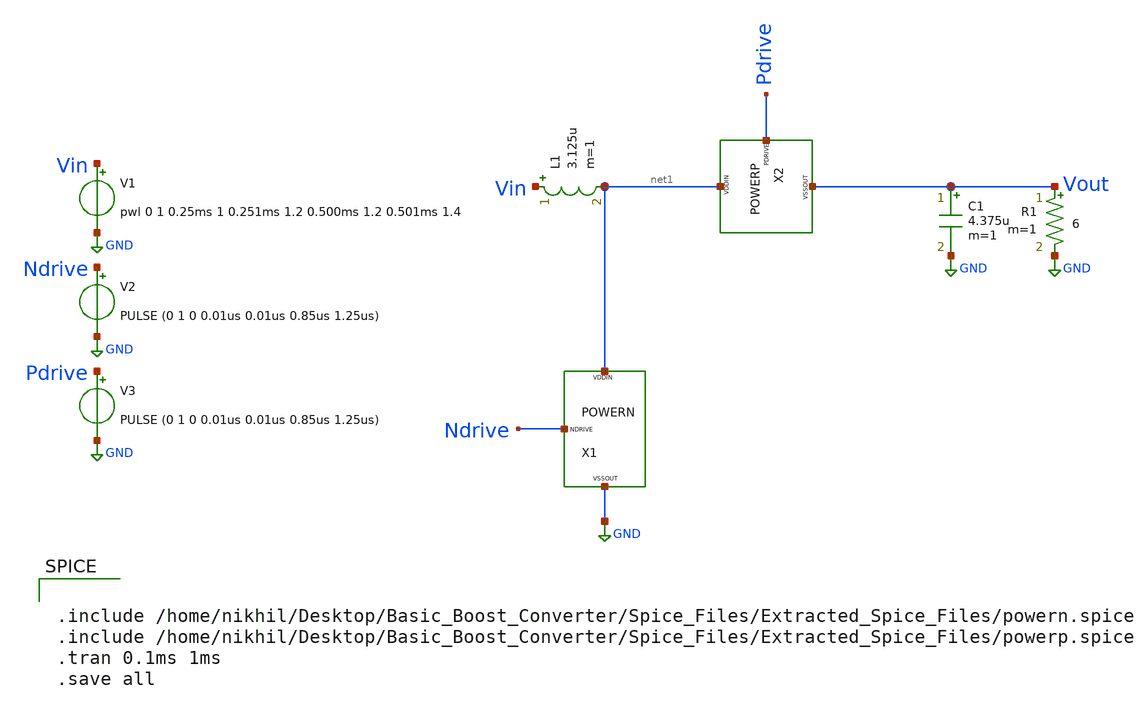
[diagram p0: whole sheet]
** sch_path: Spice_Files/Basic_Boost.sch
**.subckt Basic_Boost
C1 Vout GND 4.375u m=1
R1 Vout GND 6 m=1
L1 Vin net1 3.125u m=1
V1 Vin GND pwl 0 1 0.25ms 1 0.251ms 1.2 0.500ms 1.2 0.501ms 1.4
V2 Ndrive GND PULSE (0 1 0 0.01us 0.01us 0.85us 1.25us)
V3 Pdrive GND PULSE (0 1 0 0.01us 0.01us 0.85us 1.25us)
X1 Ndrive net1 GND powern
X2 Pdrive net1 Vout powerp
**** begin user architecture code
** manual skywater pdks install (with patches applied)
* .lib $::SKYWATER_MODELS/models/sky130.lib.spice tt_mm

** opencircuitdesign pdks install
.lib $::SKYWATER_MODELS/sky130.lib.spice tt_mm




.include /home/nikhil/Desktop/Basic_Boost_Converter/Spice_Files/Extracted_Spice_Files/powern.spice
.include /home/nikhil/Desktop/Basic_Boost_Converter/Spice_Files/Extracted_Spice_Files/powerp.spice
.tran 0.1ms 1ms
.save all

**** end user architecture code
**.ends
.GLOBAL GND
.end
